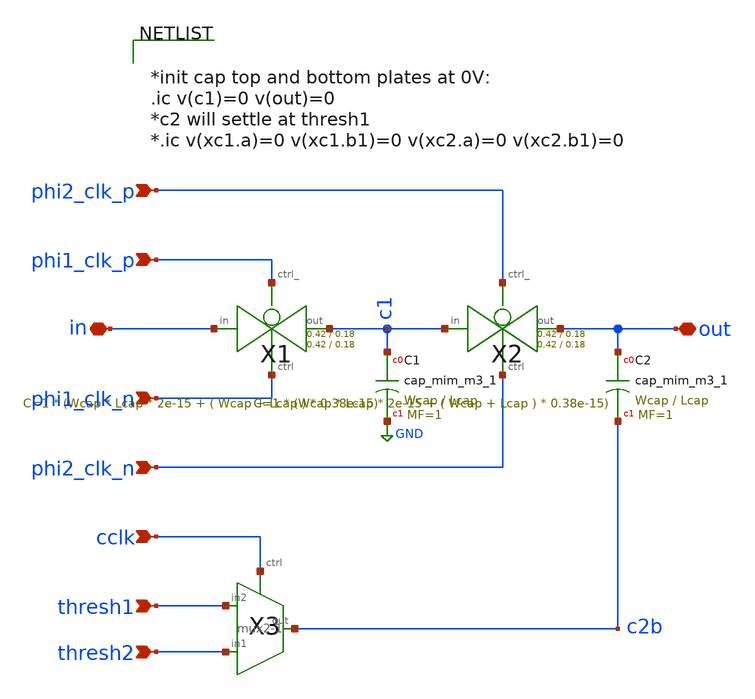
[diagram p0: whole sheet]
** sch_path: xschem/Switched_Caps/2switchcaps_thresh.sch
**.subckt 2switchcaps_thresh out in phi1_clk_n phi1_clk_p phi2_clk_p phi2_clk_n thresh1 cclk thresh2
*.iopin out
*.iopin in
*.ipin phi1_clk_n
*.ipin phi1_clk_p
*.ipin phi2_clk_p
*.ipin phi2_clk_n
*.ipin thresh1
*.ipin cclk
*.ipin thresh2
XC1 c1 GND sky130_fd_pr__cap_mim_m3_1 W=Wcap L=Lcap MF=1 m=1
XC2 out c2b sky130_fd_pr__cap_mim_m3_1 W=Wcap L=Lcap MF=1 m=1
X3 thresh2 c2b thresh1 cclk mux2-1
X1 in c1 phi1_clk_p phi1_clk_n transmission_gate Wpmos=0.42 Lpmos=0.18 Wnmos=0.42 Lnmos=0.18
X2 c1 out phi2_clk_p phi2_clk_n transmission_gate Wpmos=0.42 Lpmos=0.18 Wnmos=0.42 Lnmos=0.18
**** begin user architecture code


*init cap top and bottom plates at 0V:
.ic v(c1)=0 v(out)=0
*c2 will settle at thresh1
*.ic v(xc1.a)=0 v(xc1.b1)=0 v(xc2.a)=0 v(xc2.b1)=0


**** end user architecture code
**.ends

* expanding   symbol:  mux/mux2-1.sym # of pins=4
** sym_path: xschem/mux/mux2-1.sym
** sch_path: xschem/mux/mux2-1.sch
.subckt mux2-1 in1 out in2 ctrl
*.ipin in1
*.ipin ctrl
*.ipin in2
*.iopin out
X1 in1 out net1 ctrl transmission_gate Wpmos=3 Lpmos=0.18 Wnmos=1 Lnmos=0.18
X2 in2 out ctrl net1 transmission_gate Wpmos=3 Lpmos=0.18 Wnmos=1 Lnmos=0.18
X4 ctrl net1 inv Wpmos=3 Lpmos=0.18 Wnmos=1 Lnmos=0.18
.ends


* expanding   symbol:  transmission_gate/transmission_gate.sym # of pins=4
** sym_path: xschem/transmission_gate/transmission_gate.sym
** sch_path: xschem/transmission_gate/transmission_gate.sch
.subckt transmission_gate in out ctrl_ ctrl  Wpmos=0.42 Lpmos=0.18 Wnmos=0.42 Lnmos=0.18
*.iopin in
*.iopin out
*.ipin ctrl_
*.ipin ctrl
XM1 out ctrl in GND sky130_fd_pr__nfet_01v8 L=Lnmos W=Wnmos nf=1 ad='int((nf+1)/2) * W/nf * 0.29' as='int((nf+2)/2) * W/nf * 0.29'
+ pd='2*int((nf+1)/2) * (W/nf + 0.29)' ps='2*int((nf+2)/2) * (W/nf + 0.29)' nrd='0.29 / W' nrs='0.29 / W'
+ sa=0 sb=0 sd=0 mult=1 m=1
XM2 out ctrl_ in VDD sky130_fd_pr__pfet_01v8 L=Lpmos W=Wpmos nf=1 ad='int((nf+1)/2) * W/nf * 0.29' as='int((nf+2)/2) * W/nf * 0.29'
+ pd='2*int((nf+1)/2) * (W/nf + 0.29)' ps='2*int((nf+2)/2) * (W/nf + 0.29)' nrd='0.29 / W' nrs='0.29 / W'
+ sa=0 sb=0 sd=0 mult=1 m=1
.ends


* expanding   symbol:  inv/inv.sym # of pins=2
** sym_path: xschem/inv/inv.sym
** sch_path: xschem/inv/inv.sch
.subckt inv in out  Wpmos=3 Lpmos=0.18 Wnmos=1 Lnmos=0.18
*.ipin in
*.iopin out
XM1 out in GND GND sky130_fd_pr__nfet_01v8 L=Lnmos W=Wnmos nf=1 ad='int((nf+1)/2) * W/nf * 0.29' as='int((nf+2)/2) * W/nf * 0.29'
+ pd='2*int((nf+1)/2) * (W/nf + 0.29)' ps='2*int((nf+2)/2) * (W/nf + 0.29)' nrd='0.29 / W' nrs='0.29 / W'
+ sa=0 sb=0 sd=0 mult=1 m=1
XM2 out in VDD VDD sky130_fd_pr__pfet_01v8 L=Lpmos W=Wpmos nf=1 ad='int((nf+1)/2) * W/nf * 0.29' as='int((nf+2)/2) * W/nf * 0.29'
+ pd='2*int((nf+1)/2) * (W/nf + 0.29)' ps='2*int((nf+2)/2) * (W/nf + 0.29)' nrd='0.29 / W' nrs='0.29 / W'
+ sa=0 sb=0 sd=0 mult=1 m=1
.ends

.GLOBAL GND
.GLOBAL VDD
.end
